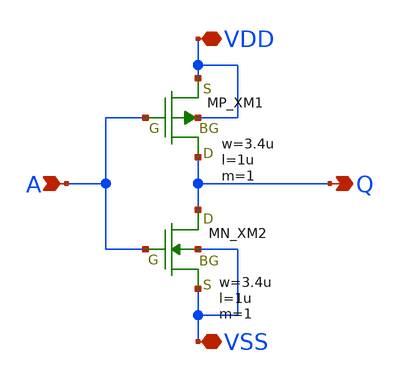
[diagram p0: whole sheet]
** sch_path: inverter/inverter_Shunsuke_Fujii.sch
**.subckt inverter_Shunsuke_Fujii A Q VDD VSS
*.ipin A
*.opin Q
*.iopin VDD
*.iopin VSS
XXM1 Q A VDD VDD PMOS w=3.4u l=1u nrd=0 nrs=0 m=1
XXM2 Q A VSS VSS NMOS w=3.4u l=1u nrd=0 nrs=0 m=1
**.ends
.end
